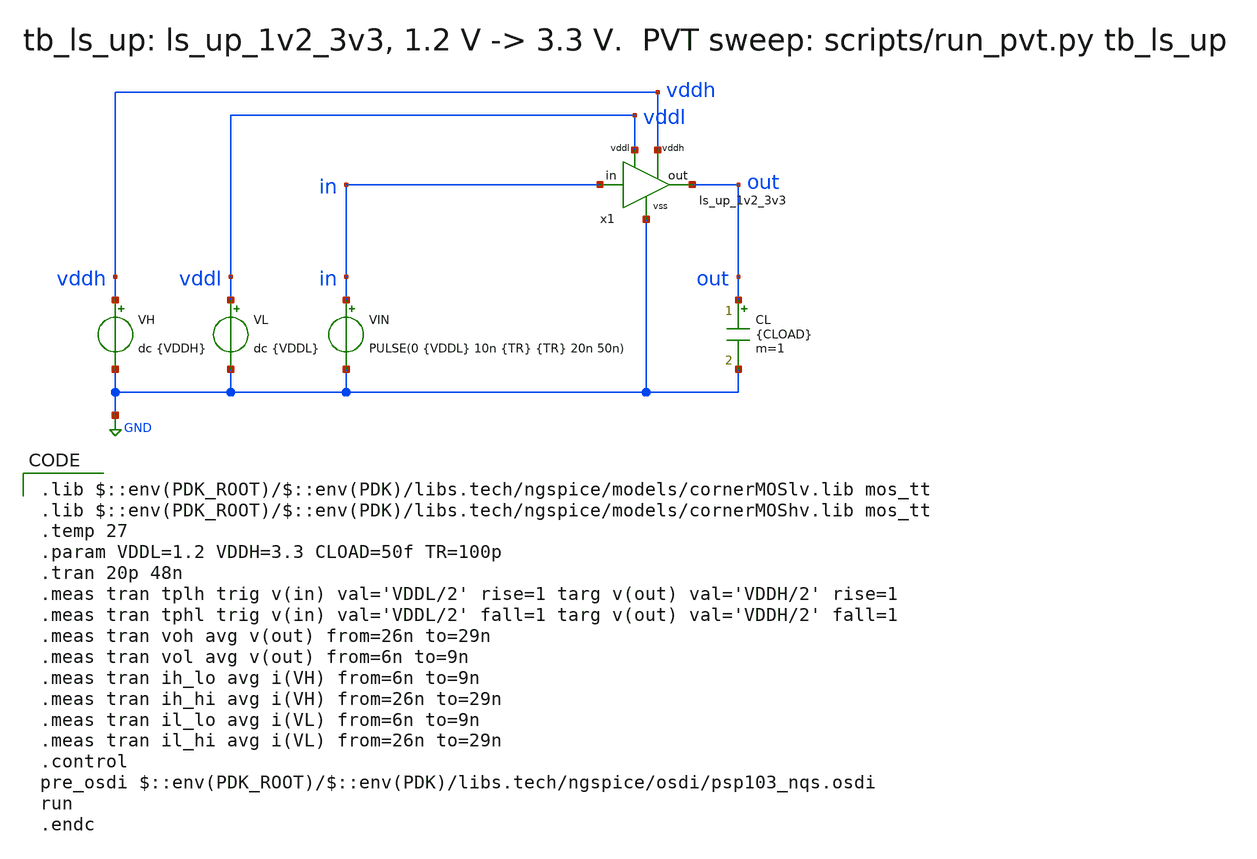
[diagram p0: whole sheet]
** sch_path: ls_pair/tb/tb_ls_up.sch
* ls_pair/xschem/ls_up_1v2_3v3.sym:
* Copyright 2023 IHP PDK Authors, Apache License 2.0 (https://www.apache.org/licenses/LICENSE-2.0)
**.subckt tb_ls_up
x1 GND vddl vddh out in ls_up_1v2_3v3
VL vddl GND dc {VDDL}
VH vddh GND dc {VDDH}
VIN in GND PULSE(0 {VDDL} 10n {TR} {TR} 20n 50n)
CL out GND {CLOAD} m=1
**** begin user architecture code
 .lib $::env(PDK_ROOT)/$::env(PDK)/libs.tech/ngspice/models/cornerMOSlv.lib mos_tt
.lib $::env(PDK_ROOT)/$::env(PDK)/libs.tech/ngspice/models/cornerMOShv.lib mos_tt
.temp 27
.param VDDL=1.2 VDDH=3.3 CLOAD=50f TR=100p
.tran 20p 48n
.meas tran tplh trig v(in) val='VDDL/2' rise=1 targ v(out) val='VDDH/2' rise=1
.meas tran tphl trig v(in) val='VDDL/2' fall=1 targ v(out) val='VDDH/2' fall=1
.meas tran voh avg v(out) from=26n to=29n
.meas tran vol avg v(out) from=6n to=9n
.meas tran ih_lo avg i(VH) from=6n to=9n
.meas tran ih_hi avg i(VH) from=26n to=29n
.meas tran il_lo avg i(VL) from=6n to=9n
.meas tran il_hi avg i(VL) from=26n to=29n
.control
pre_osdi $::env(PDK_ROOT)/$::env(PDK)/libs.tech/ngspice/osdi/psp103_nqs.osdi
run
.endc
**** end user architecture code
**.ends

* expanding   symbol:  ls_up_1v2_3v3.sym # of pins=5
** sym_path: ls_pair/xschem/ls_up_1v2_3v3.sym
** sch_path: ls_pair/xschem/ls_up_1v2_3v3.sch
.subckt ls_up_1v2_3v3 vss vddl vddh out in
*.iopin vss
*.iopin vddl
*.iopin vddh
*.opin out
*.ipin in
XM2 inb in vddl vddl sg13_lv_pmos w=1.2u l=0.13u ng=1 m=1 mm_ok=1
XM1 inb in vss vss sg13_lv_nmos w=0.6u l=0.13u ng=1 m=1 mm_ok=1
XM3 a in vss vss sg13_hv_nmos w=2u l=0.45u ng=1 m=4 mm_ok=1
XM6 a b vddh vddh sg13_hv_pmos w=2u l=0.4u ng=1 m=1 mm_ok=1
XM5 b a vddh vddh sg13_hv_pmos w=2u l=0.4u ng=1 m=1 mm_ok=1
XM4 b inb vss vss sg13_hv_nmos w=2u l=0.45u ng=1 m=4 mm_ok=1
XM16 out a vddh vddh sg13_hv_pmos w=2u l=0.4u ng=1 m=2 mm_ok=1
XM12 out a vss vss sg13_hv_nmos w=2u l=0.45u ng=1 m=1 mm_ok=1
.ends

.GLOBAL GND
.end
